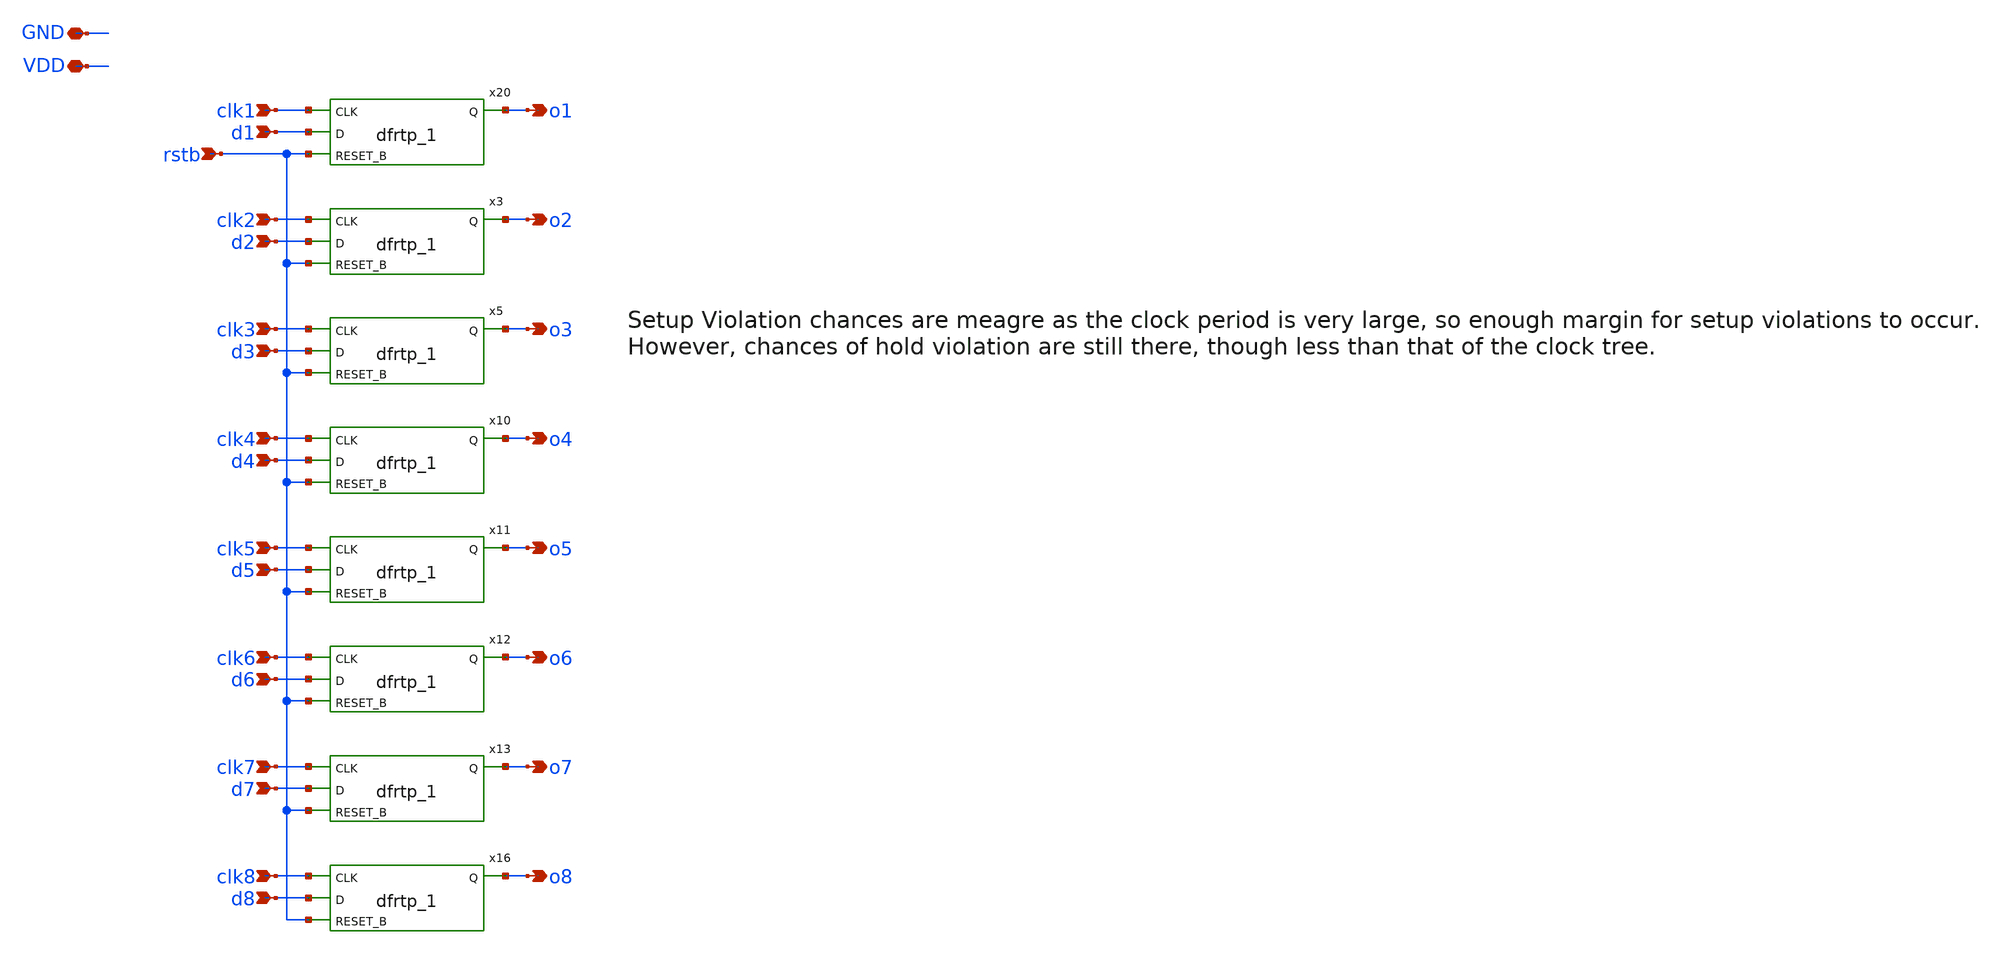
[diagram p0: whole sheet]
** sch_path: xschem/sparse_counter/sparse_counter.sch
**.subckt sparse_counter VDD GND rstb clk1 d1 clk2 clk3 clk4 clk5 clk6 clk7 clk8 d2 d3 d4 d5 d6 d7
*+ d8 o1 o2 o3 o4 o5 o6 o7 o8
*.iopin VDD
*.iopin GND
*.ipin rstb
*.ipin clk1
*.ipin d1
*.ipin clk2
*.ipin clk3
*.ipin clk4
*.ipin clk5
*.ipin clk6
*.ipin clk7
*.ipin clk8
*.ipin d2
*.ipin d3
*.ipin d4
*.ipin d5
*.ipin d6
*.ipin d7
*.ipin d8
*.opin o1
*.opin o2
*.opin o3
*.opin o4
*.opin o5
*.opin o6
*.opin o7
*.opin o8
x20 clk1 d1 rstb GND GND VDD VDD o1 sky130_fd_sc_lp__dfrtp_1
x3 clk2 d2 rstb GND GND VDD VDD o2 sky130_fd_sc_lp__dfrtp_1
x5 clk3 d3 rstb GND GND VDD VDD o3 sky130_fd_sc_lp__dfrtp_1
x10 clk4 d4 rstb GND GND VDD VDD o4 sky130_fd_sc_lp__dfrtp_1
x11 clk5 d5 rstb GND GND VDD VDD o5 sky130_fd_sc_lp__dfrtp_1
x12 clk6 d6 rstb GND GND VDD VDD o6 sky130_fd_sc_lp__dfrtp_1
x13 clk7 d7 rstb GND GND VDD VDD o7 sky130_fd_sc_lp__dfrtp_1
x16 clk8 d8 rstb GND GND VDD VDD o8 sky130_fd_sc_lp__dfrtp_1
**.ends
.end
